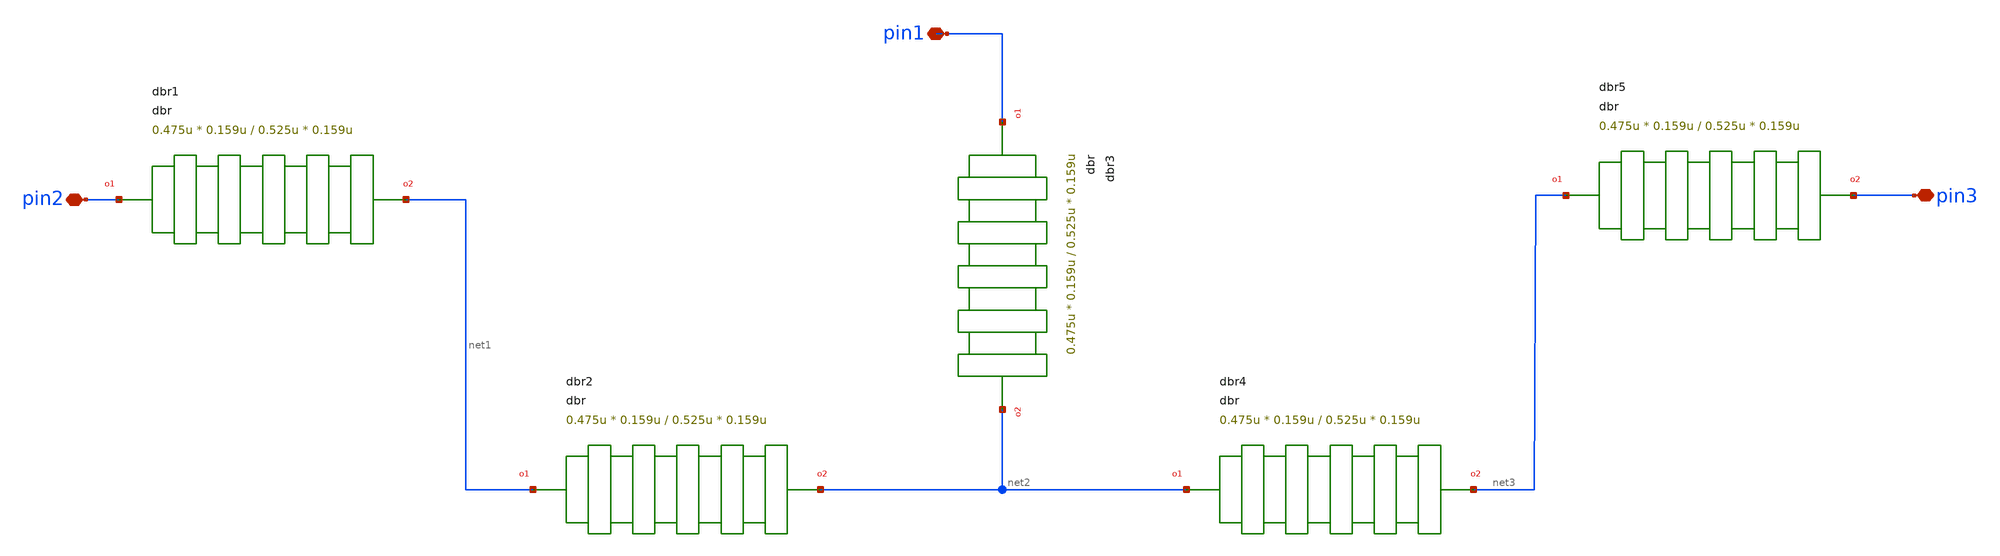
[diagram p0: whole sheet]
** sch_path: xschem/tests/test_sch/test_dbr.sch
* Copyright (c) 2024, Mabrains LLC
* Licensed under the GNU Lesser General Public License, Version 3.0 (the "License");
* you may not use this file except in compliance with the License.
* GNU Lesser General Public License
* Version 3, 29 June 2007
* This program is free software: you can redistribute it and/or modify
* it under the terms of the GNU Lesser General Public License as published
* by the Free Software Foundation, either version 3 of the License, or
* (at your option) any later version.
* This program is distributed in the hope that it will be useful,
* but WITHOUT ANY WARRANTY; without even the implied warranty of
* MERCHANTABILITY or FITNESS FOR A PARTICULAR PURPOSE.  See the
* GNU Lesser General Public License for more details.
* You should have received a copy of the GNU Lesser General Public License
* along with this program.  If not, see <https://www.gnu.org/licenses/>.
* SPDX-License-Identifier: LGPL-3.0
**.subckt test_dbr pin2 pin1 pin3
*.iopin pin2
*.iopin pin1
*.iopin pin3
Pdbr1 pin2 net1 dbr w1=0.475u l1=0.159u w2=0.525u l2=0.159u n=10
Pdbr2 net1 net2 dbr w1=0.475u l1=0.159u w2=0.525u l2=0.159u n=10
Pdbr3 pin1 net2 dbr w1=0.475u l1=0.159u w2=0.525u l2=0.159u n=10
Pdbr4 net2 net3 dbr w1=0.475u l1=0.159u w2=0.525u l2=0.159u n=10
Pdbr5 net3 pin3 dbr w1=0.475u l1=0.159u w2=0.525u l2=0.159u n=10
**.ends
.end
